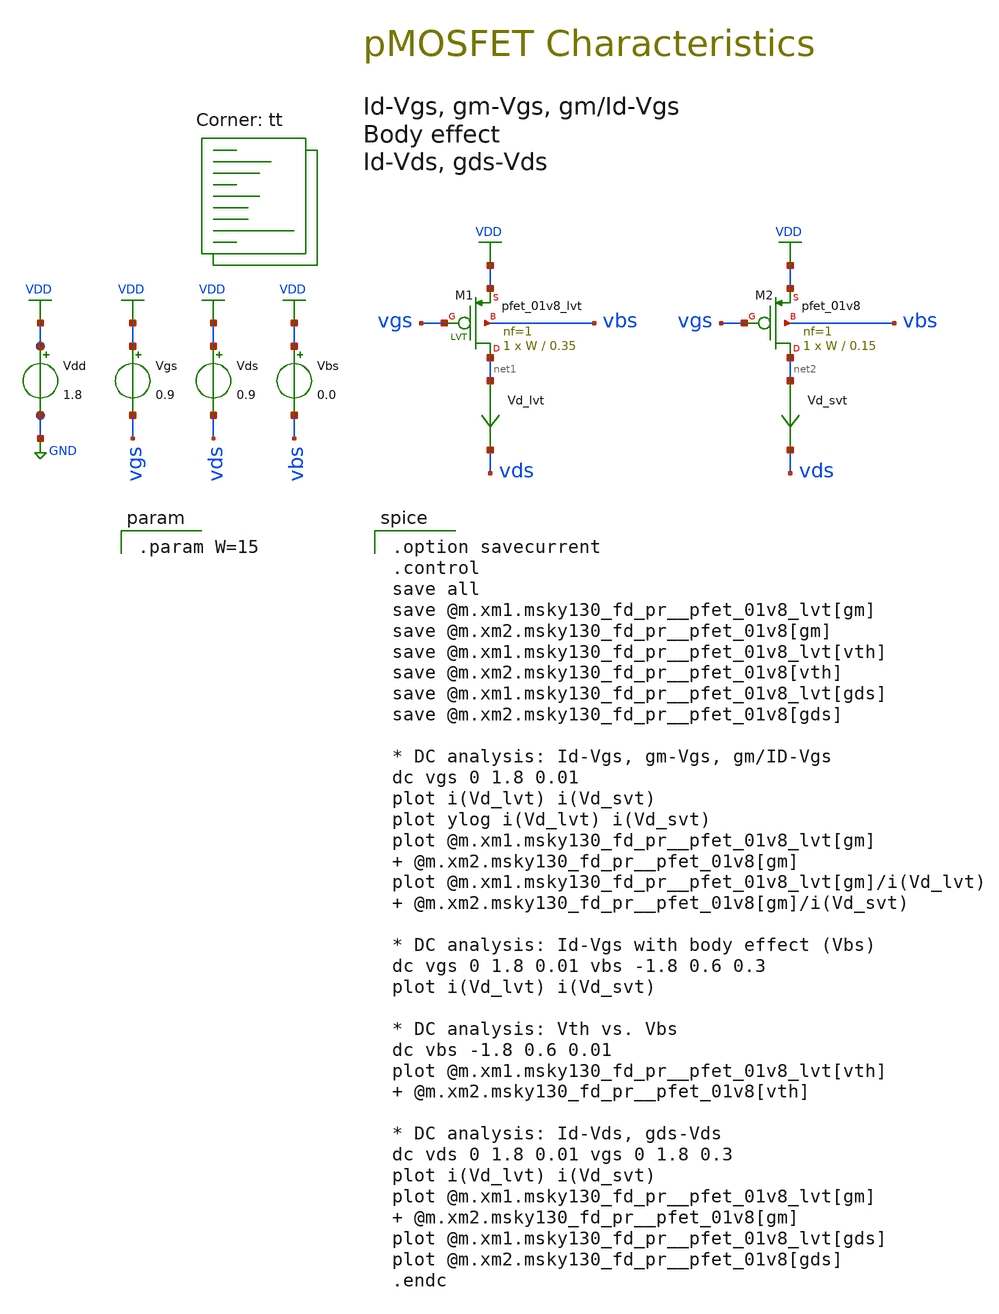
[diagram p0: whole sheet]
** sch_path: 00-b_pfet.sch
**.subckt 00-b_pfet
Vgs VDD vgs 0.9
Vds VDD vds 0.9
Vd_lvt net1 vds 0
.save i(vd_lvt)
Vbs VDD vbs 0.0
Vdd VDD GND 1.8
XM1 net1 vgs VDD vbs sky130_fd_pr__pfet_01v8_lvt L=0.35 W=W nf=1 ad='int((1 + 1)/2) * W / 1 * 0.29' as='int((1 + 2)/2) * W / 1 * 0.29'
+ pd='2*int((1 + 1)/2) * (W / 1 + 0.29)' ps='2*int((1 + 2)/2) * (W / 1 + 0.29)' nrd='0.29 / W ' nrs='0.29 / W '
+ sa=0 sb=0 sd=0 mult=1 m=1
XM2 net2 vgs VDD vbs sky130_fd_pr__pfet_01v8 L=0.15 W=W nf=1 ad='int((nf+1)/2) * W/nf * 0.29' as='int((nf+2)/2) * W/nf * 0.29'
+ pd='2*int((nf+1)/2) * (W/nf + 0.29)' ps='2*int((nf+2)/2) * (W/nf + 0.29)' nrd='0.29 / W' nrs='0.29 / W'
+ sa=0 sb=0 sd=0 mult=1 m=1
Vd_svt net2 vds 0
.save i(vd_svt)
**** begin user architecture code

.option savecurrent
.control
save all
save @m.xm1.msky130_fd_pr__pfet_01v8_lvt[gm]
save @m.xm2.msky130_fd_pr__pfet_01v8[gm]
save @m.xm1.msky130_fd_pr__pfet_01v8_lvt[vth]
save @m.xm2.msky130_fd_pr__pfet_01v8[vth]
save @m.xm1.msky130_fd_pr__pfet_01v8_lvt[gds]
save @m.xm2.msky130_fd_pr__pfet_01v8[gds]

* DC analysis: Id-Vgs, gm-Vgs, gm/ID-Vgs
dc vgs 0 1.8 0.01
plot i(Vd_lvt) i(Vd_svt)
plot ylog i(Vd_lvt) i(Vd_svt)
plot @m.xm1.msky130_fd_pr__pfet_01v8_lvt[gm]  @m.xm2.msky130_fd_pr__pfet_01v8[gm]
plot @m.xm1.msky130_fd_pr__pfet_01v8_lvt[gm]/i(Vd_lvt)
+  @m.xm2.msky130_fd_pr__pfet_01v8[gm]/i(Vd_svt)

* DC analysis: Id-Vgs with body effect (Vbs)
dc vgs 0 1.8 0.01 vbs -1.8 0.6 0.3
plot i(Vd_lvt) i(Vd_svt)

* DC analysis: Vth vs. Vbs
dc vbs -1.8 0.6 0.01
plot @m.xm1.msky130_fd_pr__pfet_01v8_lvt[vth]  @m.xm2.msky130_fd_pr__pfet_01v8[vth]

* DC analysis: Id-Vds, gds-Vds
dc vds 0 1.8 0.01 vgs 0 1.8 0.3
plot i(Vd_lvt) i(Vd_svt)
plot @m.xm1.msky130_fd_pr__pfet_01v8_lvt[gm]  @m.xm2.msky130_fd_pr__pfet_01v8[gm]
plot @m.xm1.msky130_fd_pr__pfet_01v8_lvt[gds]
plot @m.xm2.msky130_fd_pr__pfet_01v8[gds]
.endc

.lib $::SKYWATER_MODELS/sky130.lib.spice tt

.param W=15

**** end user architecture code
**.ends
.GLOBAL GND
.GLOBAL VDD
.end
